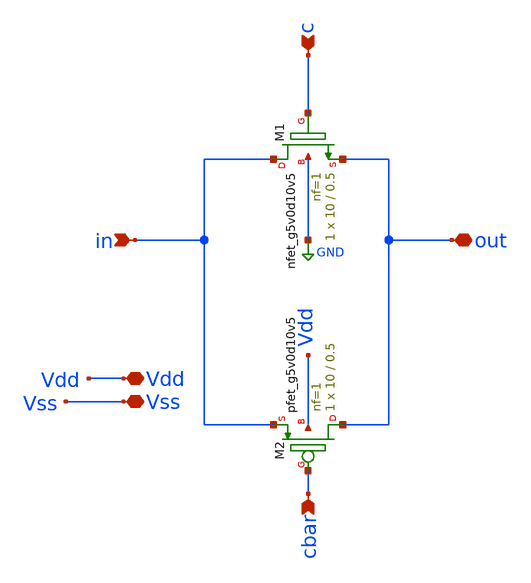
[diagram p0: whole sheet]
** sch_path: ADC/16bit_C2C/MagicAndSpice/T_gate.sch
**.subckt T_gate in cbar c Vdd Vss out
*.ipin in
*.ipin cbar
*.ipin c
*.iopin Vdd
*.iopin Vss
*.iopin out
XM1 in c out GND sky130_fd_pr__nfet_g5v0d10v5 L=0.5 W=10 nf=1 ad='int((nf+1)/2) * W/nf * 0.29' as='int((nf+2)/2) * W/nf * 0.29'
+ pd='2*int((nf+1)/2) * (W/nf + 0.29)' ps='2*int((nf+2)/2) * (W/nf + 0.29)' nrd='0.29 / W' nrs='0.29 / W'
+ sa=0 sb=0 sd=0 mult=1 m=1
XM2 out cbar in Vdd sky130_fd_pr__pfet_g5v0d10v5 L=0.5 W=10 nf=1 ad='int((nf+1)/2) * W/nf * 0.29' as='int((nf+2)/2) * W/nf * 0.29'
+ pd='2*int((nf+1)/2) * (W/nf + 0.29)' ps='2*int((nf+2)/2) * (W/nf + 0.29)' nrd='0.29 / W' nrs='0.29 / W'
+ sa=0 sb=0 sd=0 mult=1 m=1
**.ends
.GLOBAL GND
.end
